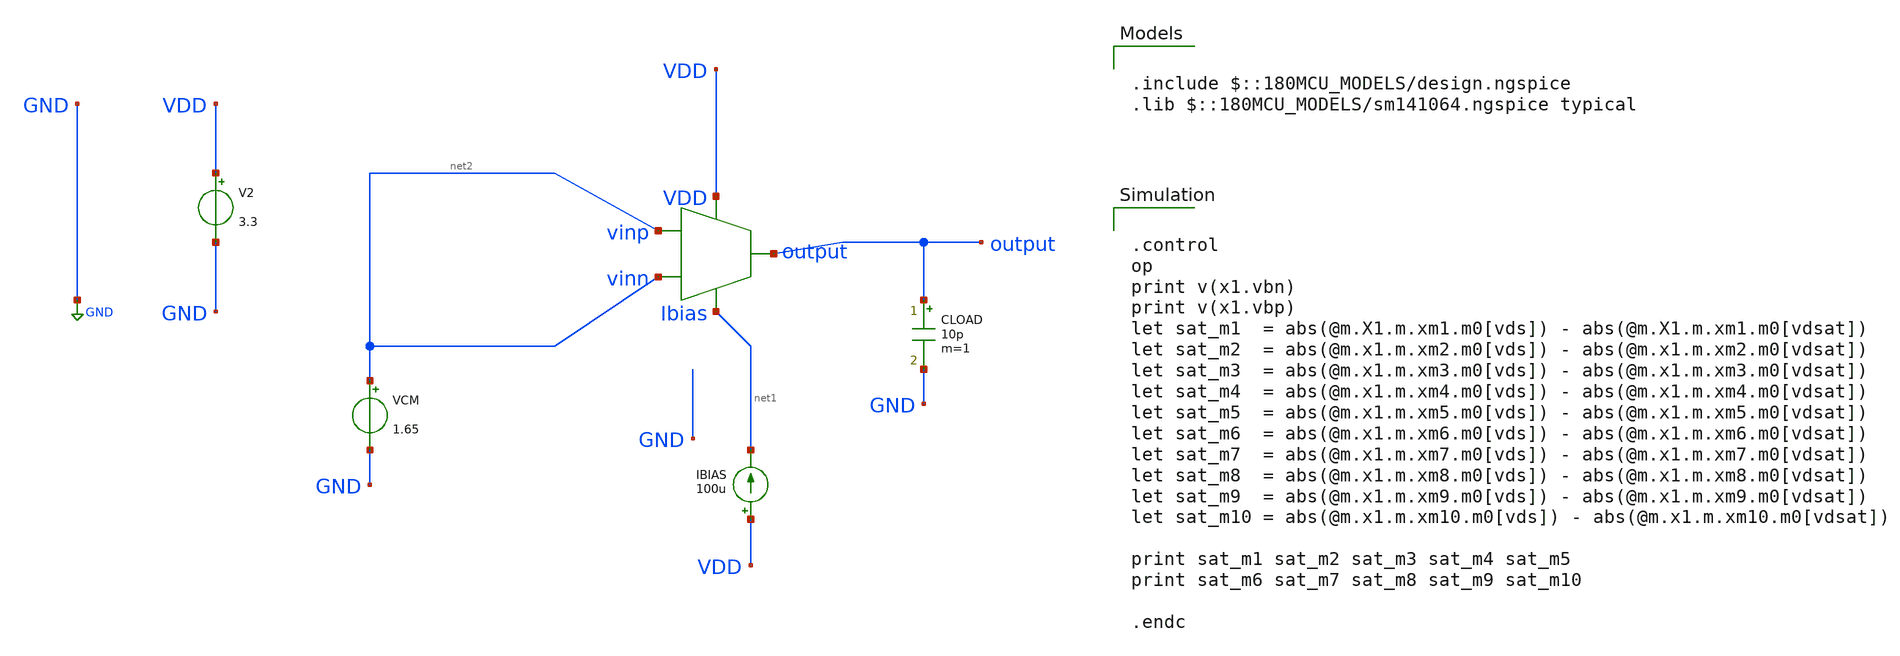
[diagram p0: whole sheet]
** sch_path: designs/libs/core_amps/ota_telescopic/telescopic_vdsat_tb.sch
**.subckt telescopic_vdsat_tb
IBIAS VDD net1 100u
V2 VDD GND 3.3
CLOAD output GND 10p m=1
VCM net2 GND 1.65
X1 net2 net2 VDD net1 output telescopic_cascode
**** begin user architecture code

.include $::180MCU_MODELS/design.ngspice
.lib $::180MCU_MODELS/sm141064.ngspice typical



.control
op
print v(x1.vbn)
print v(x1.vbp)
let sat_m1  = abs(@m.X1.m.xm1.m0[vds]) - abs(@m.X1.m.xm1.m0[vdsat])
let sat_m2  = abs(@m.x1.m.xm2.m0[vds]) - abs(@m.x1.m.xm2.m0[vdsat])
let sat_m3  = abs(@m.x1.m.xm3.m0[vds]) - abs(@m.x1.m.xm3.m0[vdsat])
let sat_m4  = abs(@m.x1.m.xm4.m0[vds]) - abs(@m.x1.m.xm4.m0[vdsat])
let sat_m5  = abs(@m.x1.m.xm5.m0[vds]) - abs(@m.x1.m.xm5.m0[vdsat])
let sat_m6  = abs(@m.x1.m.xm6.m0[vds]) - abs(@m.x1.m.xm6.m0[vdsat])
let sat_m7  = abs(@m.x1.m.xm7.m0[vds]) - abs(@m.x1.m.xm7.m0[vdsat])
let sat_m8  = abs(@m.x1.m.xm8.m0[vds]) - abs(@m.x1.m.xm8.m0[vdsat])
let sat_m9  = abs(@m.x1.m.xm9.m0[vds]) - abs(@m.x1.m.xm9.m0[vdsat])
let sat_m10 = abs(@m.x1.m.xm10.m0[vds]) - abs(@m.x1.m.xm10.m0[vdsat])

print sat_m1 sat_m2 sat_m3 sat_m4 sat_m5
print sat_m6 sat_m7 sat_m8 sat_m9 sat_m10

.endc



**** end user architecture code
**.ends

* expanding   symbol:  libs/core_amps/ota_telescopic/telescopic_cascode.sym # of pins=5
** sym_path: designs/libs/core_amps/ota_telescopic/telescopic_cascode.sym
** sch_path: designs/libs/core_amps/ota_telescopic/telescopic_cascode.sch
.subckt telescopic_cascode vinp vinn VDD Ibias output
*.ipin vinp
*.ipin vinn
*.opin output
*.iopin Ibias
*.iopin VDD
XM8 output VBP net3 VDD pfet_03v3 L=0.50u W=55u nf=1 ad='int((nf+1)/2) * W/nf * 0.18u' as='int((nf+2)/2) * W/nf * 0.18u'
+ pd='2*int((nf+1)/2) * (W/nf + 0.18u)' ps='2*int((nf+2)/2) * (W/nf + 0.18u)' nrd='0.18u / W' nrs='0.18u / W'
+ sa=0 sb=0 sd=0 m=4
XM4 output VBN net6 GND nfet_03v3 L=0.5u W=60u nf=1 ad='int((nf+1)/2) * W/nf * 0.18u' as='int((nf+2)/2) * W/nf * 0.18u'
+ pd='2*int((nf+1)/2) * (W/nf + 0.18u)' ps='2*int((nf+2)/2) * (W/nf + 0.18u)' nrd='0.18u / W' nrs='0.18u / W'
+ sa=0 sb=0 sd=0 m=3
XM1 net4 vinp net5 GND nfet_03v3 L=0.5u W=30u nf=1 ad='int((nf+1)/2) * W/nf * 0.18u' as='int((nf+2)/2) * W/nf * 0.18u'
+ pd='2*int((nf+1)/2) * (W/nf + 0.18u)' ps='2*int((nf+2)/2) * (W/nf + 0.18u)' nrd='0.18u / W' nrs='0.18u / W'
+ sa=0 sb=0 sd=0 m=1
XM2 net1 VBN net4 GND nfet_03v3 L=0.5u W=60u nf=1 ad='int((nf+1)/2) * W/nf * 0.18u' as='int((nf+2)/2) * W/nf * 0.18u'
+ pd='2*int((nf+1)/2) * (W/nf + 0.18u)' ps='2*int((nf+2)/2) * (W/nf + 0.18u)' nrd='0.18u / W' nrs='0.18u / W'
+ sa=0 sb=0 sd=0 m=3
XM3 net6 vinn net5 GND nfet_03v3 L=0.5u W=30u nf=1 ad='int((nf+1)/2) * W/nf * 0.18u' as='int((nf+2)/2) * W/nf * 0.18u'
+ pd='2*int((nf+1)/2) * (W/nf + 0.18u)' ps='2*int((nf+2)/2) * (W/nf + 0.18u)' nrd='0.18u / W' nrs='0.18u / W'
+ sa=0 sb=0 sd=0 m=1
XM5 net3 net1 VDD VDD pfet_03v3 L=0.50u W=60u nf=1 ad='int((nf+1)/2) * W/nf * 0.18u' as='int((nf+2)/2) * W/nf * 0.18u'
+ pd='2*int((nf+1)/2) * (W/nf + 0.18u)' ps='2*int((nf+2)/2) * (W/nf + 0.18u)' nrd='0.18u / W' nrs='0.18u / W'
+ sa=0 sb=0 sd=0 m=4
XM6 net1 VBP net2 VDD pfet_03v3 L=0.50u W=55u nf=1 ad='int((nf+1)/2) * W/nf * 0.18u' as='int((nf+2)/2) * W/nf * 0.18u'
+ pd='2*int((nf+1)/2) * (W/nf + 0.18u)' ps='2*int((nf+2)/2) * (W/nf + 0.18u)' nrd='0.18u / W' nrs='0.18u / W'
+ sa=0 sb=0 sd=0 m=4
XM7 net2 net1 VDD VDD pfet_03v3 L=0.50u W=60u nf=1 ad='int((nf+1)/2) * W/nf * 0.18u' as='int((nf+2)/2) * W/nf * 0.18u'
+ pd='2*int((nf+1)/2) * (W/nf + 0.18u)' ps='2*int((nf+2)/2) * (W/nf + 0.18u)' nrd='0.18u / W' nrs='0.18u / W'
+ sa=0 sb=0 sd=0 m=4
XM9 net5 Ibias GND GND nfet_03v3 L=0.5u W=60u nf=1 ad='int((nf+1)/2) * W/nf * 0.18u' as='int((nf+2)/2) * W/nf * 0.18u'
+ pd='2*int((nf+1)/2) * (W/nf + 0.18u)' ps='2*int((nf+2)/2) * (W/nf + 0.18u)' nrd='0.18u / W' nrs='0.18u / W'
+ sa=0 sb=0 sd=0 m=1
XM10 Ibias Ibias GND GND nfet_03v3 L=.5u W=20u nf=1 ad='int((nf+1)/2) * W/nf * 0.18u' as='int((nf+2)/2) * W/nf * 0.18u'
+ pd='2*int((nf+1)/2) * (W/nf + 0.18u)' ps='2*int((nf+2)/2) * (W/nf + 0.18u)' nrd='0.18u / W' nrs='0.18u / W'
+ sa=0 sb=0 sd=0 m=1
**** begin user architecture code


.include /foss/pdks/gf180mcuD/libs.tech/ngspice/design.ngspice
.lib /foss/pdks/gf180mcuD/libs.tech/ngspice/sm141064.ngspice typical

**** end user architecture code
XM11 VBN Ibias GND GND nfet_03v3 L=0.5u W=30u nf=1 ad='int((nf+1)/2) * W/nf * 0.18u' as='int((nf+2)/2) * W/nf * 0.18u'
+ pd='2*int((nf+1)/2) * (W/nf + 0.18u)' ps='2*int((nf+2)/2) * (W/nf + 0.18u)' nrd='0.18u / W' nrs='0.18u / W'
+ sa=0 sb=0 sd=0 m=1
XM12 VBP VBP GND GND nfet_03v3 L=0.5u W=1.5u nf=1 ad='int((nf+1)/2) * W/nf * 0.18u' as='int((nf+2)/2) * W/nf * 0.18u'
+ pd='2*int((nf+1)/2) * (W/nf + 0.18u)' ps='2*int((nf+2)/2) * (W/nf + 0.18u)' nrd='0.18u / W' nrs='0.18u / W'
+ sa=0 sb=0 sd=0 m=1
XM13 VBP VBN VDD VDD pfet_03v3 L=0.50u W=70u nf=1 ad='int((nf+1)/2) * W/nf * 0.18u' as='int((nf+2)/2) * W/nf * 0.18u'
+ pd='2*int((nf+1)/2) * (W/nf + 0.18u)' ps='2*int((nf+2)/2) * (W/nf + 0.18u)' nrd='0.18u / W' nrs='0.18u / W'
+ sa=0 sb=0 sd=0 m=1
XM14 VBN VBN VDD VDD pfet_03v3 L=0.50u W=70u nf=1 ad='int((nf+1)/2) * W/nf * 0.18u' as='int((nf+2)/2) * W/nf * 0.18u'
+ pd='2*int((nf+1)/2) * (W/nf + 0.18u)' ps='2*int((nf+2)/2) * (W/nf + 0.18u)' nrd='0.18u / W' nrs='0.18u / W'
+ sa=0 sb=0 sd=0 m=1
.ends

.GLOBAL GND
.end
